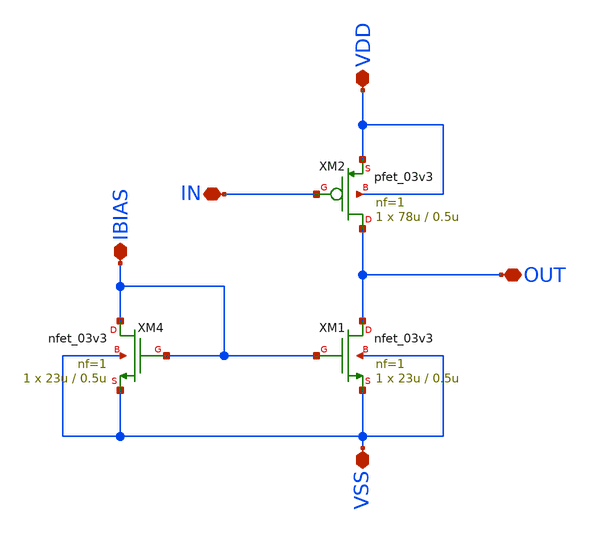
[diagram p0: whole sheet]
** sch_path: designs/libs/core_amps/cs_stage/schem/cs_schematic.sch
**.subckt cs_schematic IBIAS VDD OUT VSS IN
*.iopin IBIAS
*.iopin VDD
*.iopin OUT
*.iopin VSS
*.iopin IN
XM1 OUT IBIAS VSS VSS nfet_03v3 L=0.5u W=23u nf=1 ad='int((nf+1)/2) * W/nf * 0.18u' as='int((nf+2)/2) * W/nf * 0.18u'
+ pd='2*int((nf+1)/2) * (W/nf + 0.18u)' ps='2*int((nf+2)/2) * (W/nf + 0.18u)' nrd='0.18u / W' nrs='0.18u / W'
+ sa=0 sb=0 sd=0 m=1
XM2 OUT IN VDD VDD pfet_03v3 L=0.5u W=78u nf=1 ad='int((nf+1)/2) * W/nf * 0.18u' as='int((nf+2)/2) * W/nf * 0.18u'
+ pd='2*int((nf+1)/2) * (W/nf + 0.18u)' ps='2*int((nf+2)/2) * (W/nf + 0.18u)' nrd='0.18u / W' nrs='0.18u / W'
+ sa=0 sb=0 sd=0 m=1
XM4 IBIAS IBIAS VSS VSS nfet_03v3 L=0.5u W=23u nf=1 ad='int((nf+1)/2) * W/nf * 0.18u' as='int((nf+2)/2) * W/nf * 0.18u'
+ pd='2*int((nf+1)/2) * (W/nf + 0.18u)' ps='2*int((nf+2)/2) * (W/nf + 0.18u)' nrd='0.18u / W' nrs='0.18u / W'
+ sa=0 sb=0 sd=0 m=1
**.ends
.end
